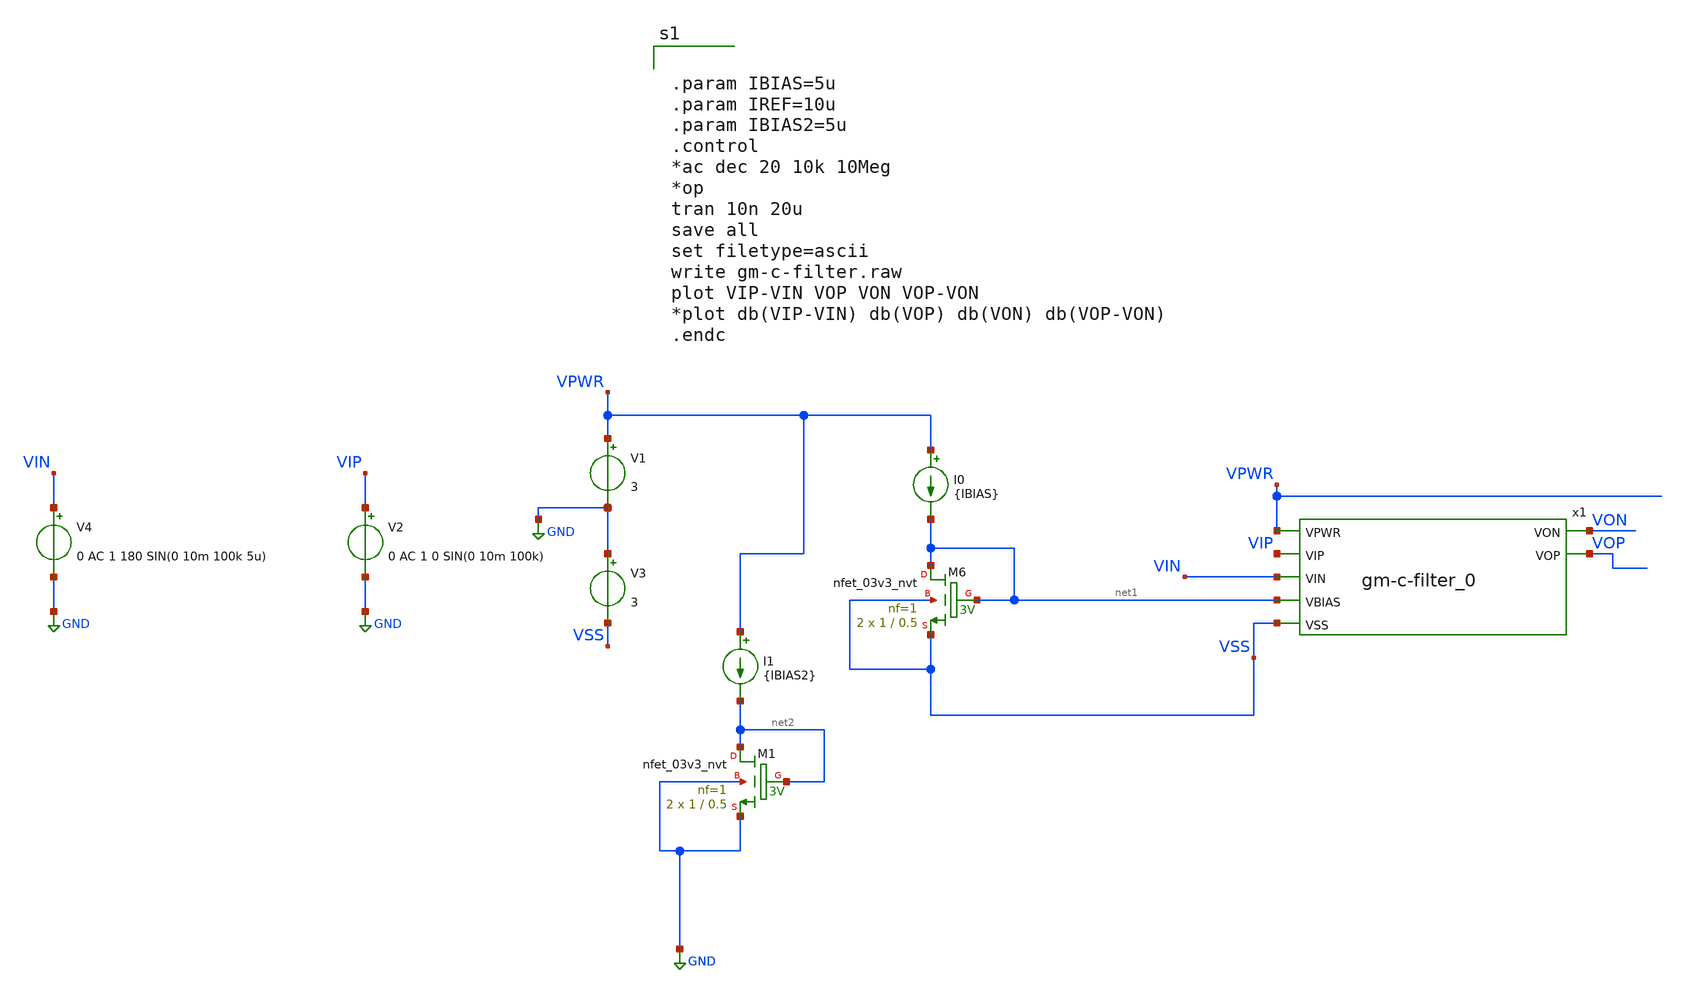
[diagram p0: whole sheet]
** sch_path: xschem/gm-c_filter/gm-c-filter_tb.sch
**.subckt gm-c-filter_tb
XM6 net1 net1 VSS VSS sky130_fd_pr__nfet_03v3_nvt L=0.5 W=1 nf=1 ad='int((nf+1)/2) * W/nf * 0.29' as='int((nf+2)/2) * W/nf * 0.29'
+ pd='2*int((nf+1)/2) * (W/nf + 0.29)' ps='2*int((nf+2)/2) * (W/nf + 0.29)' nrd='0.29 / W' nrs='0.29 / W'
+ sa=0 sb=0 sd=0 mult=2 m=2
V1 VPWR GND 3
I0 VPWR net1 {IBIAS}
V2 VIP GND 0 AC 1 0 SIN(0 10m 100k)
x1 VPWR VON VOP VIP VIN net1 VSS gm-c-filter_0
XM1 net2 net2 GND GND sky130_fd_pr__nfet_03v3_nvt L=0.5 W=1 nf=1 ad='int((nf+1)/2) * W/nf * 0.29' as='int((nf+2)/2) * W/nf * 0.29'
+ pd='2*int((nf+1)/2) * (W/nf + 0.29)' ps='2*int((nf+2)/2) * (W/nf + 0.29)' nrd='0.29 / W' nrs='0.29 / W'
+ sa=0 sb=0 sd=0 mult=2 m=2
I1 VPWR net2 {IBIAS2}
V3 GND VSS 3
V4 VIN GND 0 AC 1 180 SIN(0 10m 100k 5u)
**** begin user architecture code


.param IBIAS=5u
.param IREF=10u
.param IBIAS2=5u
.control
*ac dec 20 10k 10Meg
*op
tran 10n 20u
save all
set filetype=ascii
write gm-c-filter.raw
plot VIP-VIN VOP VON VOP-VON
*plot db(VIP-VIN) db(VOP) db(VON) db(VOP-VON)
.endc


 ** manual skywater pdks install (with patches applied)
 .lib $::SKYWATER_MODELS/sky130.lib.spice tt

** opencircuitdesign pdks install
*.lib $::SKYWATER_MODELS/sky130.lib.spice.tt.red tt

.param mc_mm_switch=0
.param mc_pr_switch=0

**** end user architecture code
**.ends

* expanding   symbol:  xschem/gm-c_filter/gm-c-filter_0.sym # of pins=7
** sym_path: xschem/gm-c_filter/gm-c-filter_0.sym
** sch_path: xschem/gm-c_filter/gm-c-filter_0.sch
.subckt gm-c-filter_0 VPWR VON VOP VIP VIN VBIAS VSS
*.ipin VBIAS
*.ipin VIP
*.ipin VPWR
*.ipin VIN
*.ipin VSS
*.opin VON
*.opin VOP
XM1 VOP VOP VPWR VPWR sky130_fd_pr__pfet_g5v0d10v5 L=0.5 W=1 nf=1 ad='int((nf+1)/2) * W/nf * 0.29' as='int((nf+2)/2) * W/nf * 0.29'
+ pd='2*int((nf+1)/2) * (W/nf + 0.29)' ps='2*int((nf+2)/2) * (W/nf + 0.29)' nrd='0.29 / W' nrs='0.29 / W'
+ sa=0 sb=0 sd=0 mult=1 m=1
XM2 VON VON VPWR VPWR sky130_fd_pr__pfet_g5v0d10v5 L=0.5 W=1 nf=1 ad='int((nf+1)/2) * W/nf * 0.29' as='int((nf+2)/2) * W/nf * 0.29'
+ pd='2*int((nf+1)/2) * (W/nf + 0.29)' ps='2*int((nf+2)/2) * (W/nf + 0.29)' nrd='0.29 / W' nrs='0.29 / W'
+ sa=0 sb=0 sd=0 mult=1 m=1
XM3 VOP VIP VTAIL VSS sky130_fd_pr__nfet_03v3_nvt L=0.5 W=1 nf=1 ad='int((nf+1)/2) * W/nf * 0.29' as='int((nf+2)/2) * W/nf * 0.29'
+ pd='2*int((nf+1)/2) * (W/nf + 0.29)' ps='2*int((nf+2)/2) * (W/nf + 0.29)' nrd='0.29 / W' nrs='0.29 / W'
+ sa=0 sb=0 sd=0 mult=1 m=1
XM4 VON VIN VTAIL VSS sky130_fd_pr__nfet_03v3_nvt L=0.5 W=1 nf=1 ad='int((nf+1)/2) * W/nf * 0.29' as='int((nf+2)/2) * W/nf * 0.29'
+ pd='2*int((nf+1)/2) * (W/nf + 0.29)' ps='2*int((nf+2)/2) * (W/nf + 0.29)' nrd='0.29 / W' nrs='0.29 / W'
+ sa=0 sb=0 sd=0 mult=1 m=1
XC1 VON VOP sky130_fd_pr__cap_mim_m3_1 W=10 L=10 MF=10 m=10
XM5 VTAIL VBIAS VSS VSS sky130_fd_pr__nfet_03v3_nvt L=0.5 W=1 nf=1 ad='int((nf+1)/2) * W/nf * 0.29' as='int((nf+2)/2) * W/nf * 0.29'
+ pd='2*int((nf+1)/2) * (W/nf + 0.29)' ps='2*int((nf+2)/2) * (W/nf + 0.29)' nrd='0.29 / W' nrs='0.29 / W'
+ sa=0 sb=0 sd=0 mult=2 m=2
.ends

.GLOBAL GND
.end
